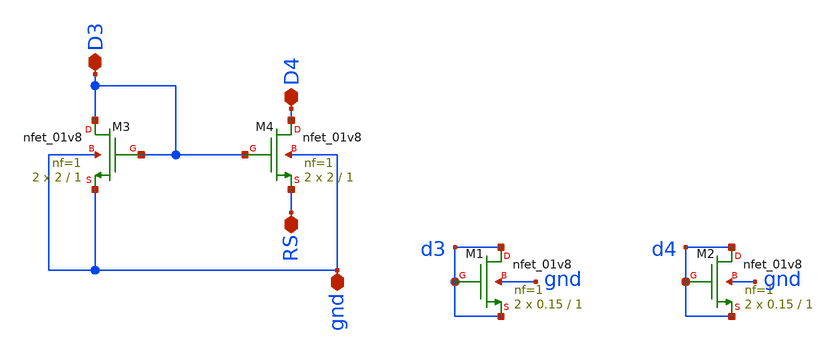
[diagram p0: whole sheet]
** sch_path: mag/nmoscs.sch
**.subckt nmoscs RS D3 D4 gnd
*.iopin RS
*.iopin D3
*.iopin D4
*.iopin gnd
XM4 D4 D3 RS gnd sky130_fd_pr__nfet_01v8 L=1 W=2 nf=1 ad='int((nf+1)/2) * W/nf * 0.29' as='int((nf+2)/2) * W/nf * 0.29'
+ pd='2*int((nf+1)/2) * (W/nf + 0.29)' ps='2*int((nf+2)/2) * (W/nf + 0.29)' nrd='0.29 / W' nrs='0.29 / W'
+ sa=0 sb=0 sd=0 mult=2 m=2
XM3 D3 D3 gnd gnd sky130_fd_pr__nfet_01v8 L=1 W=2 nf=1 ad='int((nf+1)/2) * W/nf * 0.29' as='int((nf+2)/2) * W/nf * 0.29'
+ pd='2*int((nf+1)/2) * (W/nf + 0.29)' ps='2*int((nf+2)/2) * (W/nf + 0.29)' nrd='0.29 / W' nrs='0.29 / W'
+ sa=0 sb=0 sd=0 mult=2 m=2
XM1 d3 d3 d3 gnd sky130_fd_pr__nfet_01v8 L=1 W=0.15 nf=1 ad='int((nf+1)/2) * W/nf * 0.29' as='int((nf+2)/2) * W/nf * 0.29'
+ pd='2*int((nf+1)/2) * (W/nf + 0.29)' ps='2*int((nf+2)/2) * (W/nf + 0.29)' nrd='0.29 / W' nrs='0.29 / W'
+ sa=0 sb=0 sd=0 mult=2 m=2
XM2 d4 d4 d4 gnd sky130_fd_pr__nfet_01v8 L=1 W=0.15 nf=1 ad='int((nf+1)/2) * W/nf * 0.29' as='int((nf+2)/2) * W/nf * 0.29'
+ pd='2*int((nf+1)/2) * (W/nf + 0.29)' ps='2*int((nf+2)/2) * (W/nf + 0.29)' nrd='0.29 / W' nrs='0.29 / W'
+ sa=0 sb=0 sd=0 mult=2 m=2
**.ends
.end
